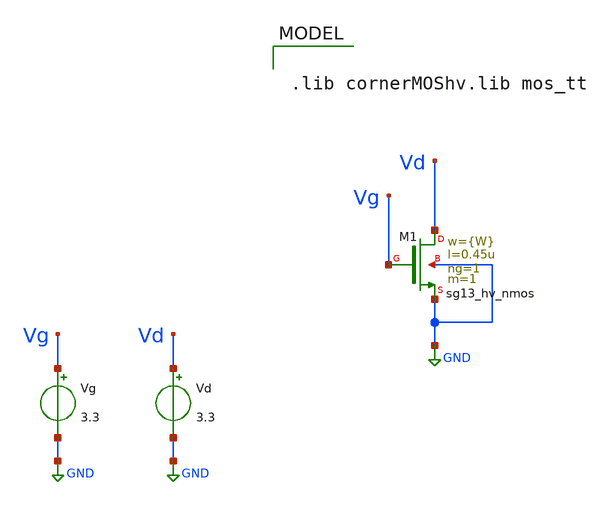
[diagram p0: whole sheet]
** sch_path: xschem/CMOS_Char/Ron_test.sch
**.subckt Ron_test
XM1 Vd Vg GND GND sg13_hv_nmos w={W} l=0.45u ng=1 m=1 mm_ok=1
Vg Vg GND 3.3
Vd Vd GND 3.3
**** begin user architecture code



.control
save all  @n.xm1.nsg13_hv_nmos[gds]
op
let rds =1/@n.xm1.nsg13_hv_nmos[gds]
print rds
.endc



.lib cornerMOShv.lib mos_tt




.param W = 1.0u
.param Vdd = 3.3


**** end user architecture code
**.ends
.GLOBAL GND
.end
